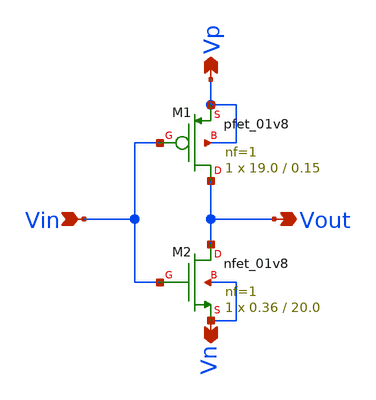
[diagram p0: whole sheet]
** sch_path: xschem/Vth_sch/Symbol/Inverter-th12.sch
**.subckt Inverter-th12 Vin Vout Vp Vn
*.ipin Vin
*.opin Vout
*.opin Vp
*.opin Vn
XM1 Vout Vin Vp Vp sky130_fd_pr__pfet_01v8 L=0.15 W=19.0 nf=1 ad='int((nf+1)/2) * W/nf * 0.29' as='int((nf+2)/2) * W/nf * 0.29'
+ pd='2*int((nf+1)/2) * (W/nf + 0.29)' ps='2*int((nf+2)/2) * (W/nf + 0.29)' nrd='0.29 / W' nrs='0.29 / W'
+ sa=0 sb=0 sd=0 mult=1 m=1
XM2 Vout Vin Vn Vn sky130_fd_pr__nfet_01v8 L=20.0 W=0.36 nf=1 ad='int((nf+1)/2) * W/nf * 0.29' as='int((nf+2)/2) * W/nf * 0.29'
+ pd='2*int((nf+1)/2) * (W/nf + 0.29)' ps='2*int((nf+2)/2) * (W/nf + 0.29)' nrd='0.29 / W' nrs='0.29 / W'
+ sa=0 sb=0 sd=0 mult=1 m=1
**.ends
.end
